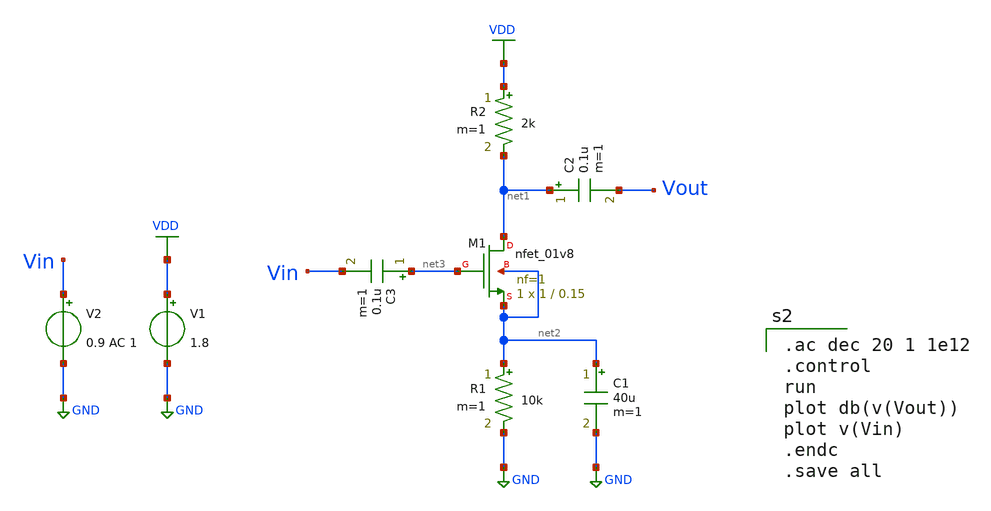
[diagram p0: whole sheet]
** sch_path: Circuits/Examples/Analog/CS_Amplifier/csamp_activeload.sch
**.subckt csamp_activeload
XM1 net1 net3 net2 net2 sky130_fd_pr__nfet_01v8 L=0.15 W=1 nf=1 ad='int((nf+1)/2) * W/nf * 0.29' as='int((nf+2)/2) * W/nf * 0.29'
+ pd='2*int((nf+1)/2) * (W/nf + 0.29)' ps='2*int((nf+2)/2) * (W/nf + 0.29)' nrd='0.29 / W' nrs='0.29 / W'
+ sa=0 sb=0 sd=0 mult=1 m=1
R1 net2 GND 10k m=1
R2 VDD net1 2k m=1
C1 net2 GND 40u m=1
C2 net1 Vout 0.1u m=1
C3 net3 Vin 0.1u m=1
V1 VDD GND 1.8
V2 Vin GND 0.9 AC 1
**** begin user architecture code
 ** manual skywater pdks install (with patches applied)
* .lib $::SKYWATER_MODELS/models/sky130.lib.spice tt

** opencircuitdesign pdks install
.lib $::SKYWATER_MODELS/sky130.lib.spice tt

.param mc_mm_switch=0
.param mc_pr_switch=0


.ac dec 20 1 1e12
.control
run
plot db(v(Vout))
plot v(Vin)
.endc
.save all

**** end user architecture code
**.ends
.GLOBAL VDD
.GLOBAL GND
.end
